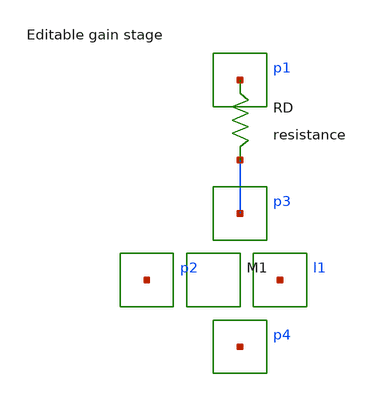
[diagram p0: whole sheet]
** sch_path: examples/xschem-amplifier/blocks/gain.sch
**.subckt gain vdd in out vss
*.ipin vdd
*.ipin in
*.opin out
*.ipin vss
RD vdd out resistance m=1
M1 out in vss vss nch w=width l=1u
**.ends
.end
